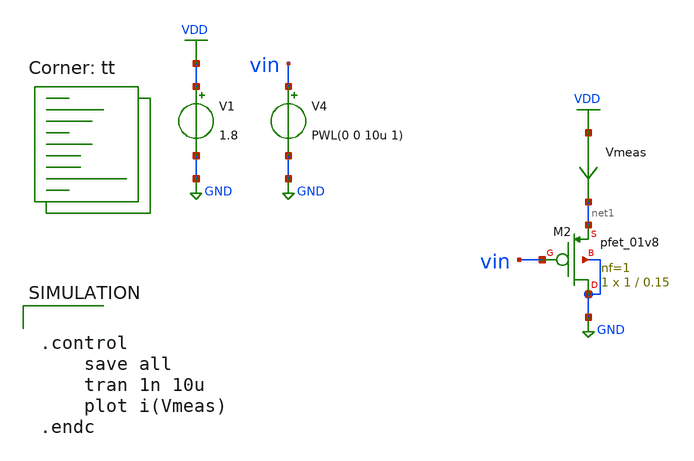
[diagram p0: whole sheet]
** sch_path: LIF_neuron/prueba.sch
**.subckt prueba
V1 VDD GND 1.8
V4 vin GND PWL(0 0 10u 1)
Vmeas VDD net1 0
.save i(vmeas)
XM2 GND vin net1 GND sky130_fd_pr__pfet_01v8 L=0.15 W=1 nf=1 ad='int((nf+1)/2) * W/nf * 0.29' as='int((nf+2)/2) * W/nf * 0.29'
+ pd='2*int((nf+1)/2) * (W/nf + 0.29)' ps='2*int((nf+2)/2) * (W/nf + 0.29)' nrd='0.29 / W' nrs='0.29 / W'
+ sa=0 sb=0 sd=0 mult=1 m=1
**** begin user architecture code
.lib $::SKYWATER_MODELS/sky130.lib.spice tt


.control
	save all
	tran 1n 10u
	plot i(Vmeas)
.endc


**** end user architecture code
**.ends
.GLOBAL GND
.GLOBAL VDD
.end
